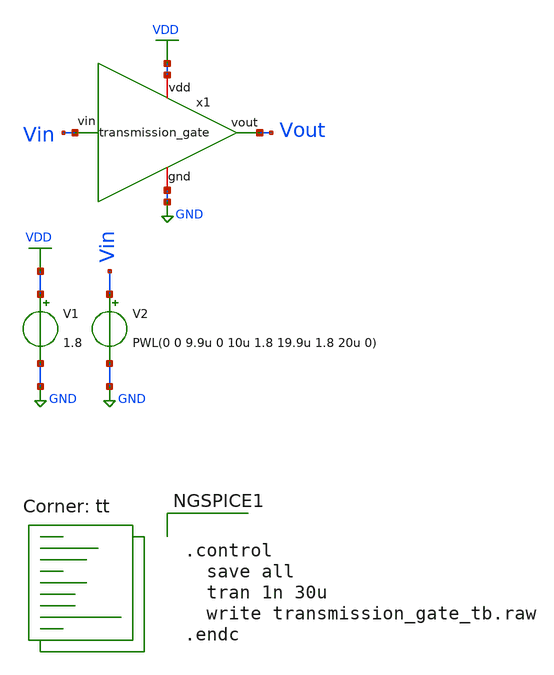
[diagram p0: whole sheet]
** sch_path: switch/transmission_gate_tb.sch
**.subckt transmission_gate_tb
x1 Vin GND VDD Vout transmission_gate
V1 VDD GND 1.8
V2 Vin GND PWL(0 0 9.9u 0 10u 1.8 19.9u 1.8 20u 0)
**** begin user architecture code
.lib $::SKYWATER_MODELS/sky130.lib.spice tt


.control
  save all
  tran 1n 30u
  write transmission_gate_tb.raw
.endc


**** end user architecture code
**.ends

* expanding   symbol:  /home/ricardo/RATT_repos/Proyectos_xschem/switch/transmission_gate.sym # of
*+ pins=4
** sym_path: switch/transmission_gate.sym
** sch_path: switch/transmission_gate.sch
.subckt transmission_gate vin gnd vdd vout
*.iopin gnd
*.iopin vdd
*.opin vout
*.ipin vin
XM1 vin net1 vout vdd sky130_fd_pr__pfet_01v8 L=0.15 W=10 nf=1 ad='int((nf+1)/2) * W/nf * 0.29' as='int((nf+2)/2) * W/nf * 0.29'
+ pd='2*int((nf+1)/2) * (W/nf + 0.29)' ps='2*int((nf+2)/2) * (W/nf + 0.29)' nrd='0.29 / W' nrs='0.29 / W'
+ sa=0 sb=0 sd=0 mult=1 m=1
XM2 vin vin vout gnd sky130_fd_pr__nfet_01v8 L=0.15 W=10 nf=1 ad='int((nf+1)/2) * W/nf * 0.29' as='int((nf+2)/2) * W/nf * 0.29'
+ pd='2*int((nf+1)/2) * (W/nf + 0.29)' ps='2*int((nf+2)/2) * (W/nf + 0.29)' nrd='0.29 / W' nrs='0.29 / W'
+ sa=0 sb=0 sd=0 mult=1 m=1
XM3 net1 vin vdd vdd sky130_fd_pr__pfet_01v8 L=0.15 W=10 nf=1 ad='int((nf+1)/2) * W/nf * 0.29' as='int((nf+2)/2) * W/nf * 0.29'
+ pd='2*int((nf+1)/2) * (W/nf + 0.29)' ps='2*int((nf+2)/2) * (W/nf + 0.29)' nrd='0.29 / W' nrs='0.29 / W'
+ sa=0 sb=0 sd=0 mult=1 m=1
XM4 net1 vin gnd gnd sky130_fd_pr__nfet_01v8 L=0.15 W=10 nf=1 ad='int((nf+1)/2) * W/nf * 0.29' as='int((nf+2)/2) * W/nf * 0.29'
+ pd='2*int((nf+1)/2) * (W/nf + 0.29)' ps='2*int((nf+2)/2) * (W/nf + 0.29)' nrd='0.29 / W' nrs='0.29 / W'
+ sa=0 sb=0 sd=0 mult=1 m=1
.ends

.GLOBAL GND
.GLOBAL VDD
.end
